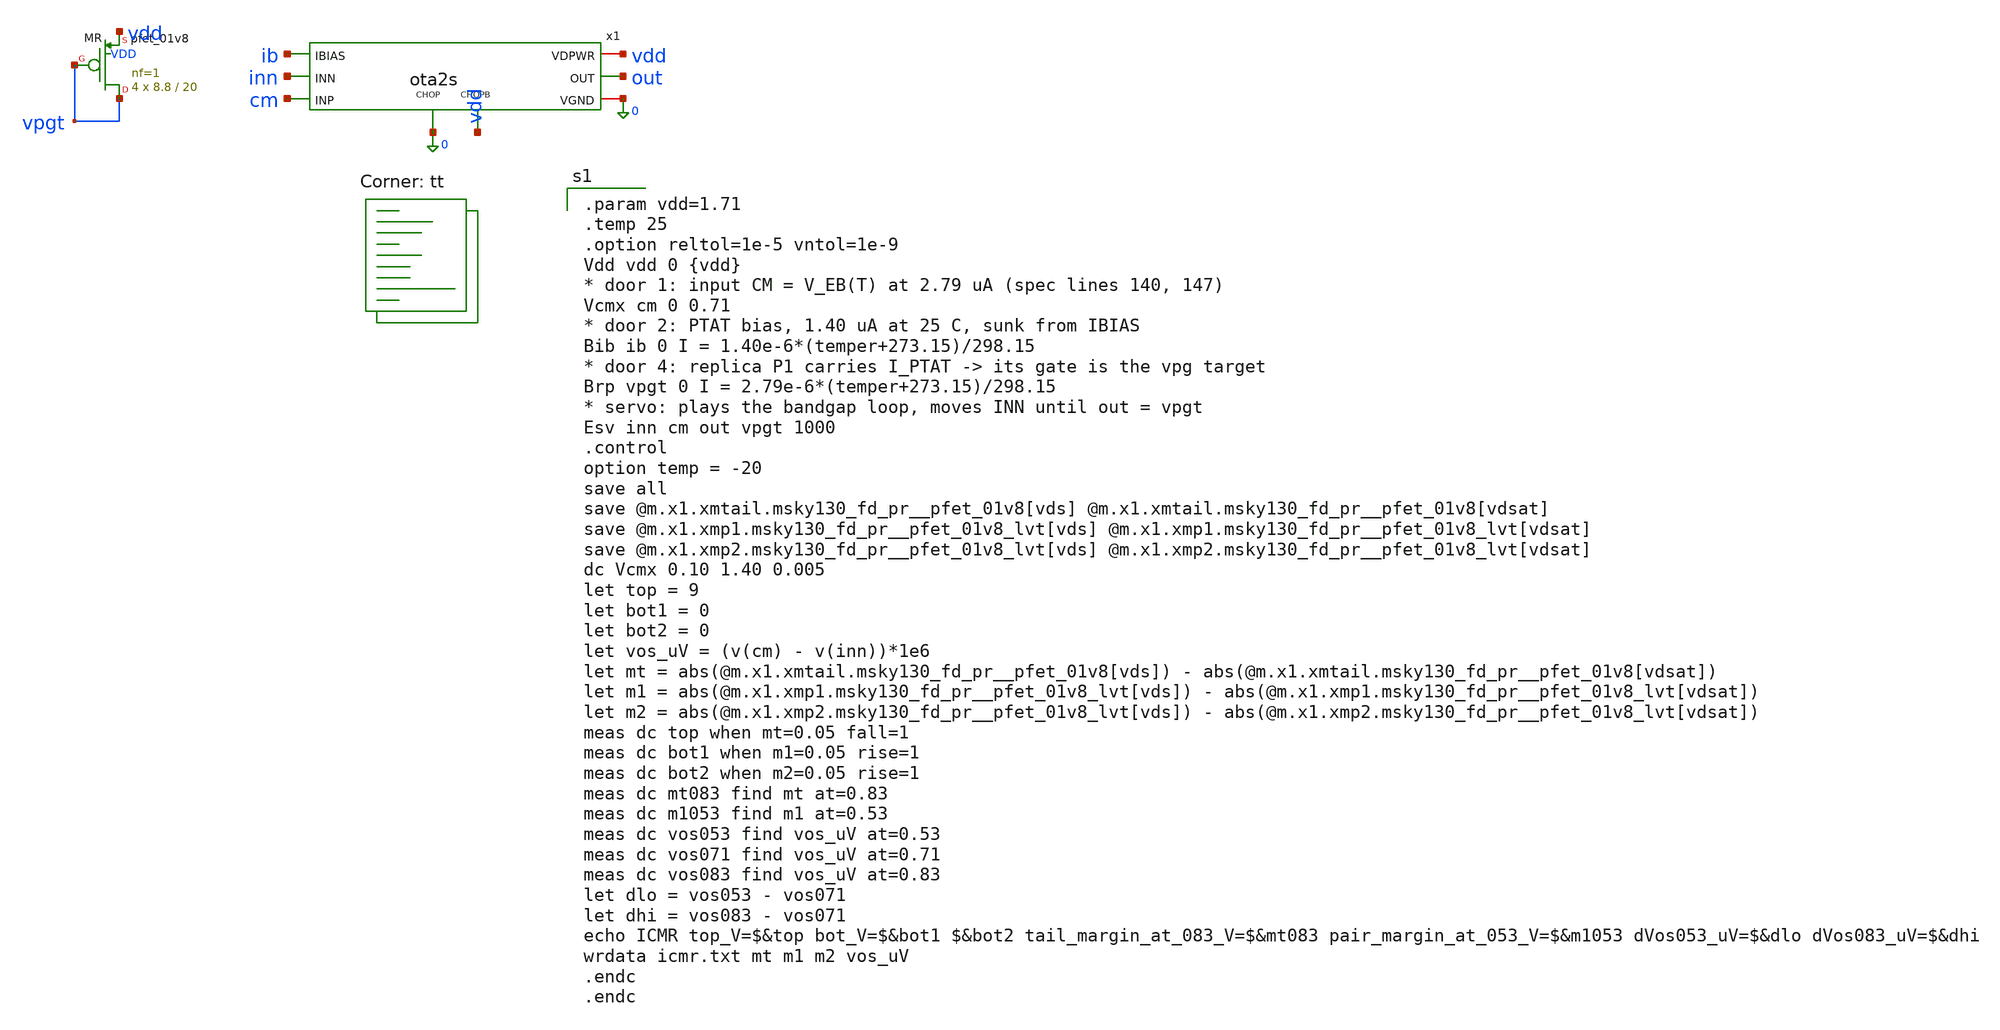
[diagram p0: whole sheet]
** sch_path: xschem/tb_ota2s_icmr.sch
**.subckt tb_ota2s_icmr
x1 cm inn out vdd 0 ib 0 vdd ota2s
XMR vpgt vpgt vdd VDD sky130_fd_pr__pfet_01v8 L=20 W=8.8 nf=1 ad='int((1 + 1)/2) * 8.8 / 1 * 0.29' as='int((1 + 2)/2) * 8.8 / 1 * 0.29'
+ pd='2*int((1 + 1)/2) * (8.8 / 1 + 0.29)' ps='2*int((1 + 2)/2) * (8.8 / 1 + 0.29)' nrd='0.29 / 8.8 ' nrs='0.29 / 8.8 '
+ sa=0 sb=0 sd=0 mult=4 m=4
**** begin user architecture code
.lib $::SKYWATER_MODELS/sky130.lib.spice tt

.param vdd=1.71
.temp 25
.option reltol=1e-5 vntol=1e-9
Vdd vdd 0 {vdd}
* door 1: input CM = V_EB(T) at 2.79 uA (spec lines 140, 147)
Vcmx cm 0 0.71
* door 2: PTAT bias, 1.40 uA at 25 C, sunk from IBIAS
Bib ib 0 I = 1.40e-6*(temper+273.15)/298.15
* door 4: replica P1 carries I_PTAT -> its gate is the vpg target
Brp vpgt 0 I = 2.79e-6*(temper+273.15)/298.15
* servo: plays the bandgap loop, moves INN until out = vpgt
Esv inn cm out vpgt 1000
.control
option temp = -20
save all
save @m.x1.xmtail.msky130_fd_pr__pfet_01v8[vds] @m.x1.xmtail.msky130_fd_pr__pfet_01v8[vdsat]
save @m.x1.xmp1.msky130_fd_pr__pfet_01v8_lvt[vds] @m.x1.xmp1.msky130_fd_pr__pfet_01v8_lvt[vdsat]
save @m.x1.xmp2.msky130_fd_pr__pfet_01v8_lvt[vds] @m.x1.xmp2.msky130_fd_pr__pfet_01v8_lvt[vdsat]
dc Vcmx 0.10 1.40 0.005
let top = 9
let bot1 = 0
let bot2 = 0
let vos_uV = (v(cm) - v(inn))*1e6
let mt = abs(@m.x1.xmtail.msky130_fd_pr__pfet_01v8[vds]) -
+ abs(@m.x1.xmtail.msky130_fd_pr__pfet_01v8[vdsat])
let m1 = abs(@m.x1.xmp1.msky130_fd_pr__pfet_01v8_lvt[vds]) -
+ abs(@m.x1.xmp1.msky130_fd_pr__pfet_01v8_lvt[vdsat])
let m2 = abs(@m.x1.xmp2.msky130_fd_pr__pfet_01v8_lvt[vds]) -
+ abs(@m.x1.xmp2.msky130_fd_pr__pfet_01v8_lvt[vdsat])
meas dc top when mt=0.05 fall=1
meas dc bot1 when m1=0.05 rise=1
meas dc bot2 when m2=0.05 rise=1
meas dc mt083 find mt at=0.83
meas dc m1053 find m1 at=0.53
meas dc vos053 find vos_uV at=0.53
meas dc vos071 find vos_uV at=0.71
meas dc vos083 find vos_uV at=0.83
let dlo = vos053 - vos071
let dhi = vos083 - vos071
echo ICMR top_V=$&top bot_V=$&bot1 $&bot2 tail_margin_at_083_V=$&mt083 pair_margin_at_053_V=$&m1053
+ dVos053_uV=$&dlo dVos083_uV=$&dhi
wrdata icmr.txt mt m1 m2 vos_uV
.endc
.endc

**** end user architecture code
**.ends

* expanding   symbol:  ota2s.sym # of pins=8
** sym_path: xschem/ota2s.sym
** sch_path: xschem/ota2s.sch
.subckt ota2s INP INN OUT VDPWR VGND IBIAS CHOP CHOPB
*.ipin INN
*.ipin INP
*.ipin IBIAS
*.opin OUT
*.iopin VDPWR
*.iopin VGND
*.ipin CHOPB
*.ipin CHOP
XMREF IBIAS IBIAS VDPWR VDPWR sky130_fd_pr__pfet_01v8 L=4 W=20 nf=1 ad='int((1 + 1)/2) * 20 / 1 * 0.29'
+ as='int((1 + 2)/2) * 20 / 1 * 0.29' pd='2*int((1 + 1)/2) * (20 / 1 + 0.29)' ps='2*int((1 + 2)/2) * (20 / 1 + 0.29)'
+ nrd='0.29 / 20 ' nrs='0.29 / 20 ' sa=0 sb=0 sd=0 mult=1 m=1
XMTAIL tail IBIAS VDPWR VDPWR sky130_fd_pr__pfet_01v8 L=4 W=20 nf=1 ad='int((1 + 1)/2) * 20 / 1 * 0.29'
+ as='int((1 + 2)/2) * 20 / 1 * 0.29' pd='2*int((1 + 1)/2) * (20 / 1 + 0.29)' ps='2*int((1 + 2)/2) * (20 / 1 + 0.29)'
+ nrd='0.29 / 20 ' nrs='0.29 / 20 ' sa=0 sb=0 sd=0 mult=2 m=2
XMP1 d1 INN tail VDPWR sky130_fd_pr__pfet_01v8_lvt L=6 W=25 nf=1 ad='int((1 + 1)/2) * 25 / 1 * 0.29'
+ as='int((1 + 2)/2) * 25 / 1 * 0.29' pd='2*int((1 + 1)/2) * (25 / 1 + 0.29)' ps='2*int((1 + 2)/2) * (25 / 1 + 0.29)'
+ nrd='0.29 / 25 ' nrs='0.29 / 25 ' sa=0 sb=0 sd=0 mult=24 m=24
XMP2 x1 INP tail VDPWR sky130_fd_pr__pfet_01v8_lvt L=6 W=25 nf=1 ad='int((1 + 1)/2) * 25 / 1 * 0.29'
+ as='int((1 + 2)/2) * 25 / 1 * 0.29' pd='2*int((1 + 1)/2) * (25 / 1 + 0.29)' ps='2*int((1 + 2)/2) * (25 / 1 + 0.29)'
+ nrd='0.29 / 25 ' nrs='0.29 / 25 ' sa=0 sb=0 sd=0 mult=24 m=24
XMN1 d1 g12 VGND VGND sky130_fd_pr__nfet_01v8 L=20 W=6 nf=1 ad='int((1 + 1)/2) * 6 / 1 * 0.29' as='int((1 + 2)/2) * 6 / 1 * 0.29'
+ pd='2*int((1 + 1)/2) * (6 / 1 + 0.29)' ps='2*int((1 + 2)/2) * (6 / 1 + 0.29)' nrd='0.29 / 6 ' nrs='0.29 / 6 '
+ sa=0 sb=0 sd=0 mult=2 m=2
XMN2 x1 g12 VGND VGND sky130_fd_pr__nfet_01v8 L=20 W=6 nf=1 ad='int((1 + 1)/2) * 6 / 1 * 0.29' as='int((1 + 2)/2) * 6 / 1 * 0.29'
+ pd='2*int((1 + 1)/2) * (6 / 1 + 0.29)' ps='2*int((1 + 2)/2) * (6 / 1 + 0.29)' nrd='0.29 / 6 ' nrs='0.29 / 6 '
+ sa=0 sb=0 sd=0 mult=2 m=2
XMP3 OUT IBIAS VDPWR VDPWR sky130_fd_pr__pfet_01v8 L=4 W=20 nf=1 ad='int((1 + 1)/2) * 20 / 1 * 0.29'
+ as='int((1 + 2)/2) * 20 / 1 * 0.29' pd='2*int((1 + 1)/2) * (20 / 1 + 0.29)' ps='2*int((1 + 2)/2) * (20 / 1 + 0.29)'
+ nrd='0.29 / 20 ' nrs='0.29 / 20 ' sa=0 sb=0 sd=0 mult=6 m=6
XMN3 OUT g3 VGND VGND sky130_fd_pr__nfet_01v8 L=1 W=7 nf=1 ad='int((1 + 1)/2) * 7 / 1 * 0.29' as='int((1 + 2)/2) * 7 / 1 * 0.29'
+ pd='2*int((1 + 1)/2) * (7 / 1 + 0.29)' ps='2*int((1 + 2)/2) * (7 / 1 + 0.29)' nrd='0.29 / 7 ' nrs='0.29 / 7 '
+ sa=0 sb=0 sd=0 mult=1 m=1
XRZ1 net1 g3 VGND sky130_fd_pr__res_high_po_1p41 L=20 mult=1 m=1
XRZ2 net2 net1 VGND sky130_fd_pr__res_high_po_1p41 L=20 mult=1 m=1
XRZ3 net3 net2 VGND sky130_fd_pr__res_high_po_1p41 L=20 mult=1 m=1
XRZ4 net4 net3 VGND sky130_fd_pr__res_high_po_1p41 L=20 mult=1 m=1
XRZ5 net5 net4 VGND sky130_fd_pr__res_high_po_1p41 L=20 mult=1 m=1
XRZ6 cz net5 VGND sky130_fd_pr__res_high_po_1p41 L=20 mult=1 m=1
XCC cz OUT sky130_fd_pr__cap_mim_m3_1 W=25 L=25 MF=8 m=8
XDP tail VDPWR tail VDPWR sky130_fd_pr__pfet_01v8_lvt L=6 W=25 nf=1 ad='int((1 + 1)/2) * 25 / 1 * 0.29'
+ as='int((1 + 2)/2) * 25 / 1 * 0.29' pd='2*int((1 + 1)/2) * (25 / 1 + 0.29)' ps='2*int((1 + 2)/2) * (25 / 1 + 0.29)'
+ nrd='0.29 / 25 ' nrs='0.29 / 25 ' sa=0 sb=0 sd=0 mult=8 m=8
XDNA d1 VGND VGND VGND sky130_fd_pr__nfet_01v8 L=20 W=6 nf=1 ad='int((1 + 1)/2) * 6 / 1 * 0.29' as='int((1 + 2)/2) * 6 / 1 * 0.29'
+ pd='2*int((1 + 1)/2) * (6 / 1 + 0.29)' ps='2*int((1 + 2)/2) * (6 / 1 + 0.29)' nrd='0.29 / 6 ' nrs='0.29 / 6 '
+ sa=0 sb=0 sd=0 mult=2 m=2
XDNB x1 VGND VGND VGND sky130_fd_pr__nfet_01v8 L=20 W=6 nf=1 ad='int((1 + 1)/2) * 6 / 1 * 0.29' as='int((1 + 2)/2) * 6 / 1 * 0.29'
+ pd='2*int((1 + 1)/2) * (6 / 1 + 0.29)' ps='2*int((1 + 2)/2) * (6 / 1 + 0.29)' nrd='0.29 / 6 ' nrs='0.29 / 6 '
+ sa=0 sb=0 sd=0 mult=2 m=2
XDB VDPWR VDPWR VDPWR VDPWR sky130_fd_pr__pfet_01v8 L=4 W=20 nf=1 ad='int((1 + 1)/2) * 20 / 1 * 0.29'
+ as='int((1 + 2)/2) * 20 / 1 * 0.29' pd='2*int((1 + 1)/2) * (20 / 1 + 0.29)' ps='2*int((1 + 2)/2) * (20 / 1 + 0.29)'
+ nrd='0.29 / 20 ' nrs='0.29 / 20 ' sa=0 sb=0 sd=0 mult=2 m=2
XRD1 VGND VGND VGND sky130_fd_pr__res_high_po_1p41 L=20 mult=1 m=1
XRD2 VGND VGND VGND sky130_fd_pr__res_high_po_1p41 L=20 mult=1 m=1
XSD1 d1 CHOPB g12 VGND sky130_fd_pr__nfet_01v8 L=0.5 W=6 nf=1 ad='int((1 + 1)/2) * 6 / 1 * 0.29' as='int((1 + 2)/2) * 6 / 1 * 0.29'
+ pd='2*int((1 + 1)/2) * (6 / 1 + 0.29)' ps='2*int((1 + 2)/2) * (6 / 1 + 0.29)' nrd='0.29 / 6 ' nrs='0.29 / 6 '
+ sa=0 sb=0 sd=0 mult=1 m=1
XSD2 x1 CHOP g12 VGND sky130_fd_pr__nfet_01v8 L=0.5 W=6 nf=1 ad='int((1 + 1)/2) * 6 / 1 * 0.29' as='int((1 + 2)/2) * 6 / 1 * 0.29'
+ pd='2*int((1 + 1)/2) * (6 / 1 + 0.29)' ps='2*int((1 + 2)/2) * (6 / 1 + 0.29)' nrd='0.29 / 6 ' nrs='0.29 / 6 '
+ sa=0 sb=0 sd=0 mult=1 m=1
XSG2 g3 CHOP d1 VGND sky130_fd_pr__nfet_01v8 L=0.5 W=6 nf=1 ad='int((1 + 1)/2) * 6 / 1 * 0.29' as='int((1 + 2)/2) * 6 / 1 * 0.29'
+ pd='2*int((1 + 1)/2) * (6 / 1 + 0.29)' ps='2*int((1 + 2)/2) * (6 / 1 + 0.29)' nrd='0.29 / 6 ' nrs='0.29 / 6 '
+ sa=0 sb=0 sd=0 mult=1 m=1
XSG1 x1 CHOPB g3 VGND sky130_fd_pr__nfet_01v8 L=0.5 W=6 nf=1 ad='int((1 + 1)/2) * 6 / 1 * 0.29' as='int((1 + 2)/2) * 6 / 1 * 0.29'
+ pd='2*int((1 + 1)/2) * (6 / 1 + 0.29)' ps='2*int((1 + 2)/2) * (6 / 1 + 0.29)' nrd='0.29 / 6 ' nrs='0.29 / 6 '
+ sa=0 sb=0 sd=0 mult=1 m=1
.ends

.end
